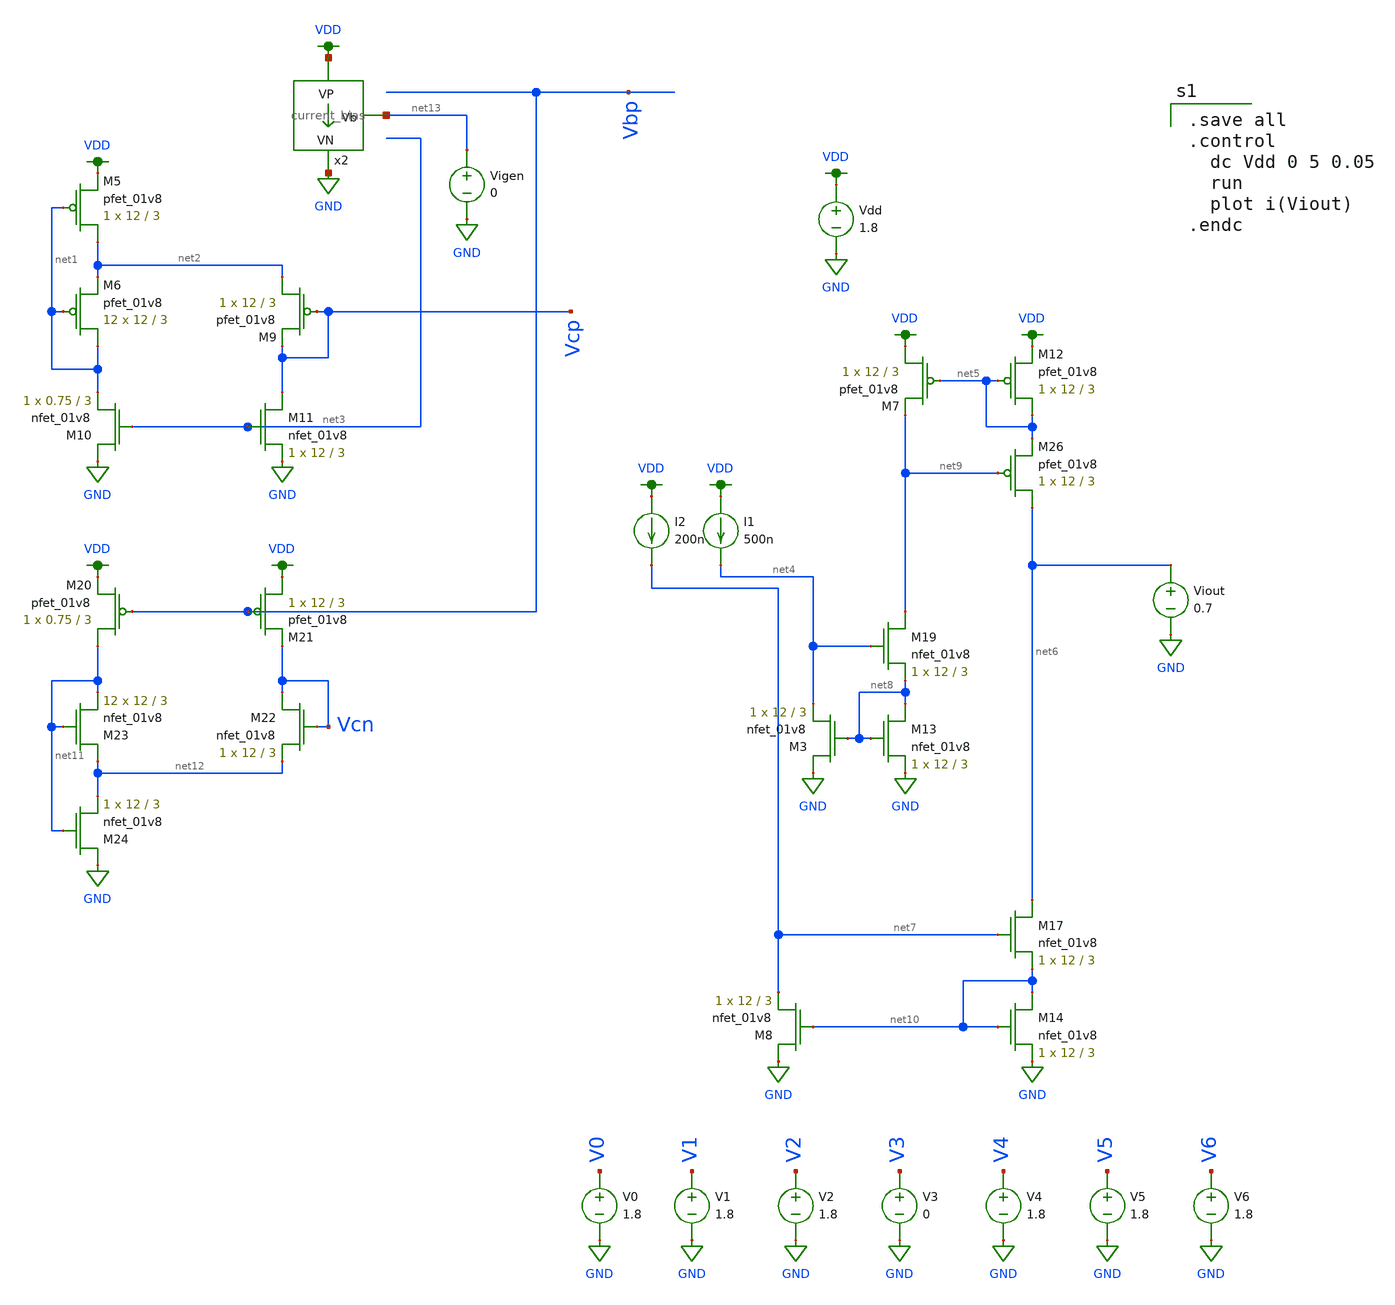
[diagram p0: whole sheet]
** sch_path: schematics/ieee DAC/ieee_DAC_mc_simulation_6.sch
**.subckt ieee_DAC_mc_simulation_6
Vdd VDD GND 1.8
V1 V1 GND 1.8
V2 V2 GND 1.8
V3 V3 GND 0
V4 V4 GND 1.8
V5 V5 GND 1.8
V6 V6 GND 1.8
V0 V0 GND 1.8
XM5 net2 net1 VDD VDD sky130_fd_pr__pfet_01v8 L=3 W=12 nf=1 ad='int((nf+1)/2) * W/nf * 0.29' as='int((nf+2)/2) * W/nf * 0.29'
+ pd='2*int((nf+1)/2) * (W/nf + 0.29)' ps='2*int((nf+2)/2) * (W/nf + 0.29)' nrd='0.29 / W' nrs='0.29 / W'
+ sa=0 sb=0 sd=0 mult=1 m=1
XM6 net1 net1 net2 VDD sky130_fd_pr__pfet_01v8 L=3 W=12 nf=1 ad='int((nf+1)/2) * W/nf * 0.29' as='int((nf+2)/2) * W/nf * 0.29'
+ pd='2*int((nf+1)/2) * (W/nf + 0.29)' ps='2*int((nf+2)/2) * (W/nf + 0.29)' nrd='0.29 / W' nrs='0.29 / W'
+ sa=0 sb=0 sd=0 mult=12 m=12
XM9 net2 Vcp Vcp VDD sky130_fd_pr__pfet_01v8 L=3 W=12 nf=1 ad='int((nf+1)/2) * W/nf * 0.29' as='int((nf+2)/2) * W/nf * 0.29'
+ pd='2*int((nf+1)/2) * (W/nf + 0.29)' ps='2*int((nf+2)/2) * (W/nf + 0.29)' nrd='0.29 / W' nrs='0.29 / W'
+ sa=0 sb=0 sd=0 mult=1 m=1
XM10 GND net3 net1 GND sky130_fd_pr__nfet_01v8 L=3 W=0.75 nf=1 ad='int((nf+1)/2) * W/nf * 0.29' as='int((nf+2)/2) * W/nf * 0.29'
+ pd='2*int((nf+1)/2) * (W/nf + 0.29)' ps='2*int((nf+2)/2) * (W/nf + 0.29)' nrd='0.29 / W' nrs='0.29 / W'
+ sa=0 sb=0 sd=0 mult=1 m=1
XM11 Vcp net3 GND GND sky130_fd_pr__nfet_01v8 L=3 W=12 nf=1 ad='int((nf+1)/2) * W/nf * 0.29' as='int((nf+2)/2) * W/nf * 0.29'
+ pd='2*int((nf+1)/2) * (W/nf + 0.29)' ps='2*int((nf+2)/2) * (W/nf + 0.29)' nrd='0.29 / W' nrs='0.29 / W'
+ sa=0 sb=0 sd=0 mult=1 m=1
x2 VDD net13 GND current_bias
Vigen net13 GND 0
XM3 GND net8 net4 GND sky130_fd_pr__nfet_01v8 L=3 W=12 nf=1 ad='int((nf+1)/2) * W/nf * 0.29' as='int((nf+2)/2) * W/nf * 0.29'
+ pd='2*int((nf+1)/2) * (W/nf + 0.29)' ps='2*int((nf+2)/2) * (W/nf + 0.29)' nrd='0.29 / W' nrs='0.29 / W'
+ sa=0 sb=0 sd=0 mult=1 m=1
XM7 VDD net5 net9 VDD sky130_fd_pr__pfet_01v8 L=3 W=12 nf=1 ad='int((nf+1)/2) * W/nf * 0.29' as='int((nf+2)/2) * W/nf * 0.29'
+ pd='2*int((nf+1)/2) * (W/nf + 0.29)' ps='2*int((nf+2)/2) * (W/nf + 0.29)' nrd='0.29 / W' nrs='0.29 / W'
+ sa=0 sb=0 sd=0 mult=1 m=1
XM8 GND net10 net7 GND sky130_fd_pr__nfet_01v8 L=3 W=12 nf=1 ad='int((nf+1)/2) * W/nf * 0.29' as='int((nf+2)/2) * W/nf * 0.29'
+ pd='2*int((nf+1)/2) * (W/nf + 0.29)' ps='2*int((nf+2)/2) * (W/nf + 0.29)' nrd='0.29 / W' nrs='0.29 / W'
+ sa=0 sb=0 sd=0 mult=1 m=1
XM12 net5 net5 VDD VDD sky130_fd_pr__pfet_01v8 L=3 W=12 nf=1 ad='int((nf+1)/2) * W/nf * 0.29' as='int((nf+2)/2) * W/nf * 0.29'
+ pd='2*int((nf+1)/2) * (W/nf + 0.29)' ps='2*int((nf+2)/2) * (W/nf + 0.29)' nrd='0.29 / W' nrs='0.29 / W'
+ sa=0 sb=0 sd=0 mult=1 m=1
Viout net6 GND 0.7
XM13 net8 net8 GND GND sky130_fd_pr__nfet_01v8 L=3 W=12 nf=1 ad='int((nf+1)/2) * W/nf * 0.29' as='int((nf+2)/2) * W/nf * 0.29'
+ pd='2*int((nf+1)/2) * (W/nf + 0.29)' ps='2*int((nf+2)/2) * (W/nf + 0.29)' nrd='0.29 / W' nrs='0.29 / W'
+ sa=0 sb=0 sd=0 mult=1 m=1
XM14 net10 net10 GND GND sky130_fd_pr__nfet_01v8 L=3 W=12 nf=1 ad='int((nf+1)/2) * W/nf * 0.29' as='int((nf+2)/2) * W/nf * 0.29'
+ pd='2*int((nf+1)/2) * (W/nf + 0.29)' ps='2*int((nf+2)/2) * (W/nf + 0.29)' nrd='0.29 / W' nrs='0.29 / W'
+ sa=0 sb=0 sd=0 mult=1 m=1
XM20 net11 Vbp VDD VDD sky130_fd_pr__pfet_01v8 L=3 W=0.75 nf=1 ad='int((nf+1)/2) * W/nf * 0.29' as='int((nf+2)/2) * W/nf * 0.29'
+ pd='2*int((nf+1)/2) * (W/nf + 0.29)' ps='2*int((nf+2)/2) * (W/nf + 0.29)' nrd='0.29 / W' nrs='0.29 / W'
+ sa=0 sb=0 sd=0 mult=1 m=1
XM21 VDD Vbp Vcn VDD sky130_fd_pr__pfet_01v8 L=3 W=12 nf=1 ad='int((nf+1)/2) * W/nf * 0.29' as='int((nf+2)/2) * W/nf * 0.29'
+ pd='2*int((nf+1)/2) * (W/nf + 0.29)' ps='2*int((nf+2)/2) * (W/nf + 0.29)' nrd='0.29 / W' nrs='0.29 / W'
+ sa=0 sb=0 sd=0 mult=1 m=1
XM22 Vcn Vcn net12 GND sky130_fd_pr__nfet_01v8 L=3 W=12 nf=1 ad='int((nf+1)/2) * W/nf * 0.29' as='int((nf+2)/2) * W/nf * 0.29'
+ pd='2*int((nf+1)/2) * (W/nf + 0.29)' ps='2*int((nf+2)/2) * (W/nf + 0.29)' nrd='0.29 / W' nrs='0.29 / W'
+ sa=0 sb=0 sd=0 mult=1 m=1
XM23 net12 net11 net11 GND sky130_fd_pr__nfet_01v8 L=3 W=12 nf=1 ad='int((nf+1)/2) * W/nf * 0.29' as='int((nf+2)/2) * W/nf * 0.29'
+ pd='2*int((nf+1)/2) * (W/nf + 0.29)' ps='2*int((nf+2)/2) * (W/nf + 0.29)' nrd='0.29 / W' nrs='0.29 / W'
+ sa=0 sb=0 sd=0 mult=12 m=12
XM24 GND net11 net12 GND sky130_fd_pr__nfet_01v8 L=3 W=12 nf=1 ad='int((nf+1)/2) * W/nf * 0.29' as='int((nf+2)/2) * W/nf * 0.29'
+ pd='2*int((nf+1)/2) * (W/nf + 0.29)' ps='2*int((nf+2)/2) * (W/nf + 0.29)' nrd='0.29 / W' nrs='0.29 / W'
+ sa=0 sb=0 sd=0 mult=1 m=1
XM17 net6 net7 net10 GND sky130_fd_pr__nfet_01v8 L=3 W=12 nf=1 ad='int((nf+1)/2) * W/nf * 0.29' as='int((nf+2)/2) * W/nf * 0.29'
+ pd='2*int((nf+1)/2) * (W/nf + 0.29)' ps='2*int((nf+2)/2) * (W/nf + 0.29)' nrd='0.29 / W' nrs='0.29 / W'
+ sa=0 sb=0 sd=0 mult=1 m=1
XM19 net9 net4 net8 GND sky130_fd_pr__nfet_01v8 L=3 W=12 nf=1 ad='int((nf+1)/2) * W/nf * 0.29' as='int((nf+2)/2) * W/nf * 0.29'
+ pd='2*int((nf+1)/2) * (W/nf + 0.29)' ps='2*int((nf+2)/2) * (W/nf + 0.29)' nrd='0.29 / W' nrs='0.29 / W'
+ sa=0 sb=0 sd=0 mult=1 m=1
XM26 net6 net9 net5 VDD sky130_fd_pr__pfet_01v8 L=3 W=12 nf=1 ad='int((nf+1)/2) * W/nf * 0.29' as='int((nf+2)/2) * W/nf * 0.29'
+ pd='2*int((nf+1)/2) * (W/nf + 0.29)' ps='2*int((nf+2)/2) * (W/nf + 0.29)' nrd='0.29 / W' nrs='0.29 / W'
+ sa=0 sb=0 sd=0 mult=1 m=1
I1 VDD net4 500n
I2 VDD net7 200n
**** begin user architecture code

.option wnflag=1
.param MC_SWITCH=1.0
.lib ~/skywater/skywater-pdk/libraries/sky130_fd_pr_ngspice/latest/models/sky130.lib.spice tt


.save all
.control
  dc Vdd 0 5 0.05
  run
  plot i(Viout)
.endc

**** end user architecture code
**.ends
.GLOBAL VDD
.GLOBAL GND
.end
